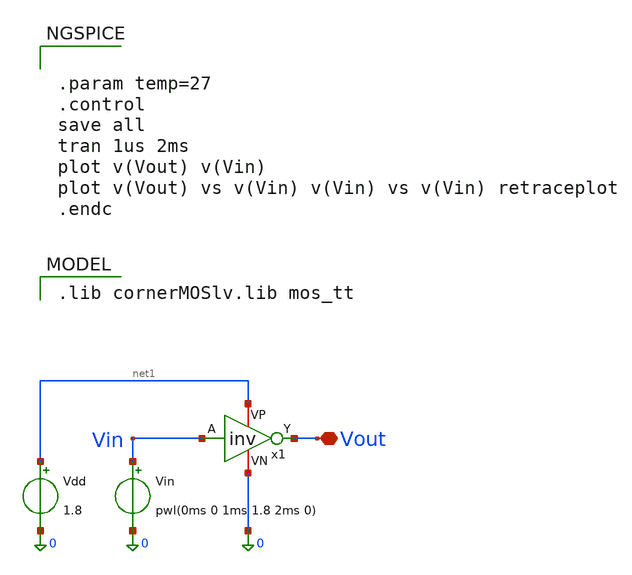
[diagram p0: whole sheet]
** sch_path: xschem/inv_tb.sch
**.subckt inv_tb Vout
*.iopin Vout
x1 net1 Vin Vout 0 inv
Vin Vin 0 pwl(0ms 0 1ms 1.8 2ms 0)
Vdd net1 0 1.8
**** begin user architecture code
 .lib cornerMOSlv.lib mos_tt



.param temp=27
.control
save all
tran 1us 2ms
plot v(Vout) v(Vin)
plot v(Vout) vs v(Vin) v(Vin) vs v(Vin) retraceplot
.endc


**** end user architecture code
**.ends

* expanding   symbol:  inv.sym # of pins=4
** sym_path: xschem/inv.sym
** sch_path: xschem/inv.sch
.subckt inv VP A Y VN
*.ipin A
*.opin Y
*.iopin VP
*.iopin VN
XM1 Y A VN VN sg13_lv_nmos w=1u l=0.13u ng=1 m=1 mm_ok=1
XM2 Y A VP VP sg13_lv_pmos w=1u l=0.13u ng=1 m=1 mm_ok=1
.ends

.end
